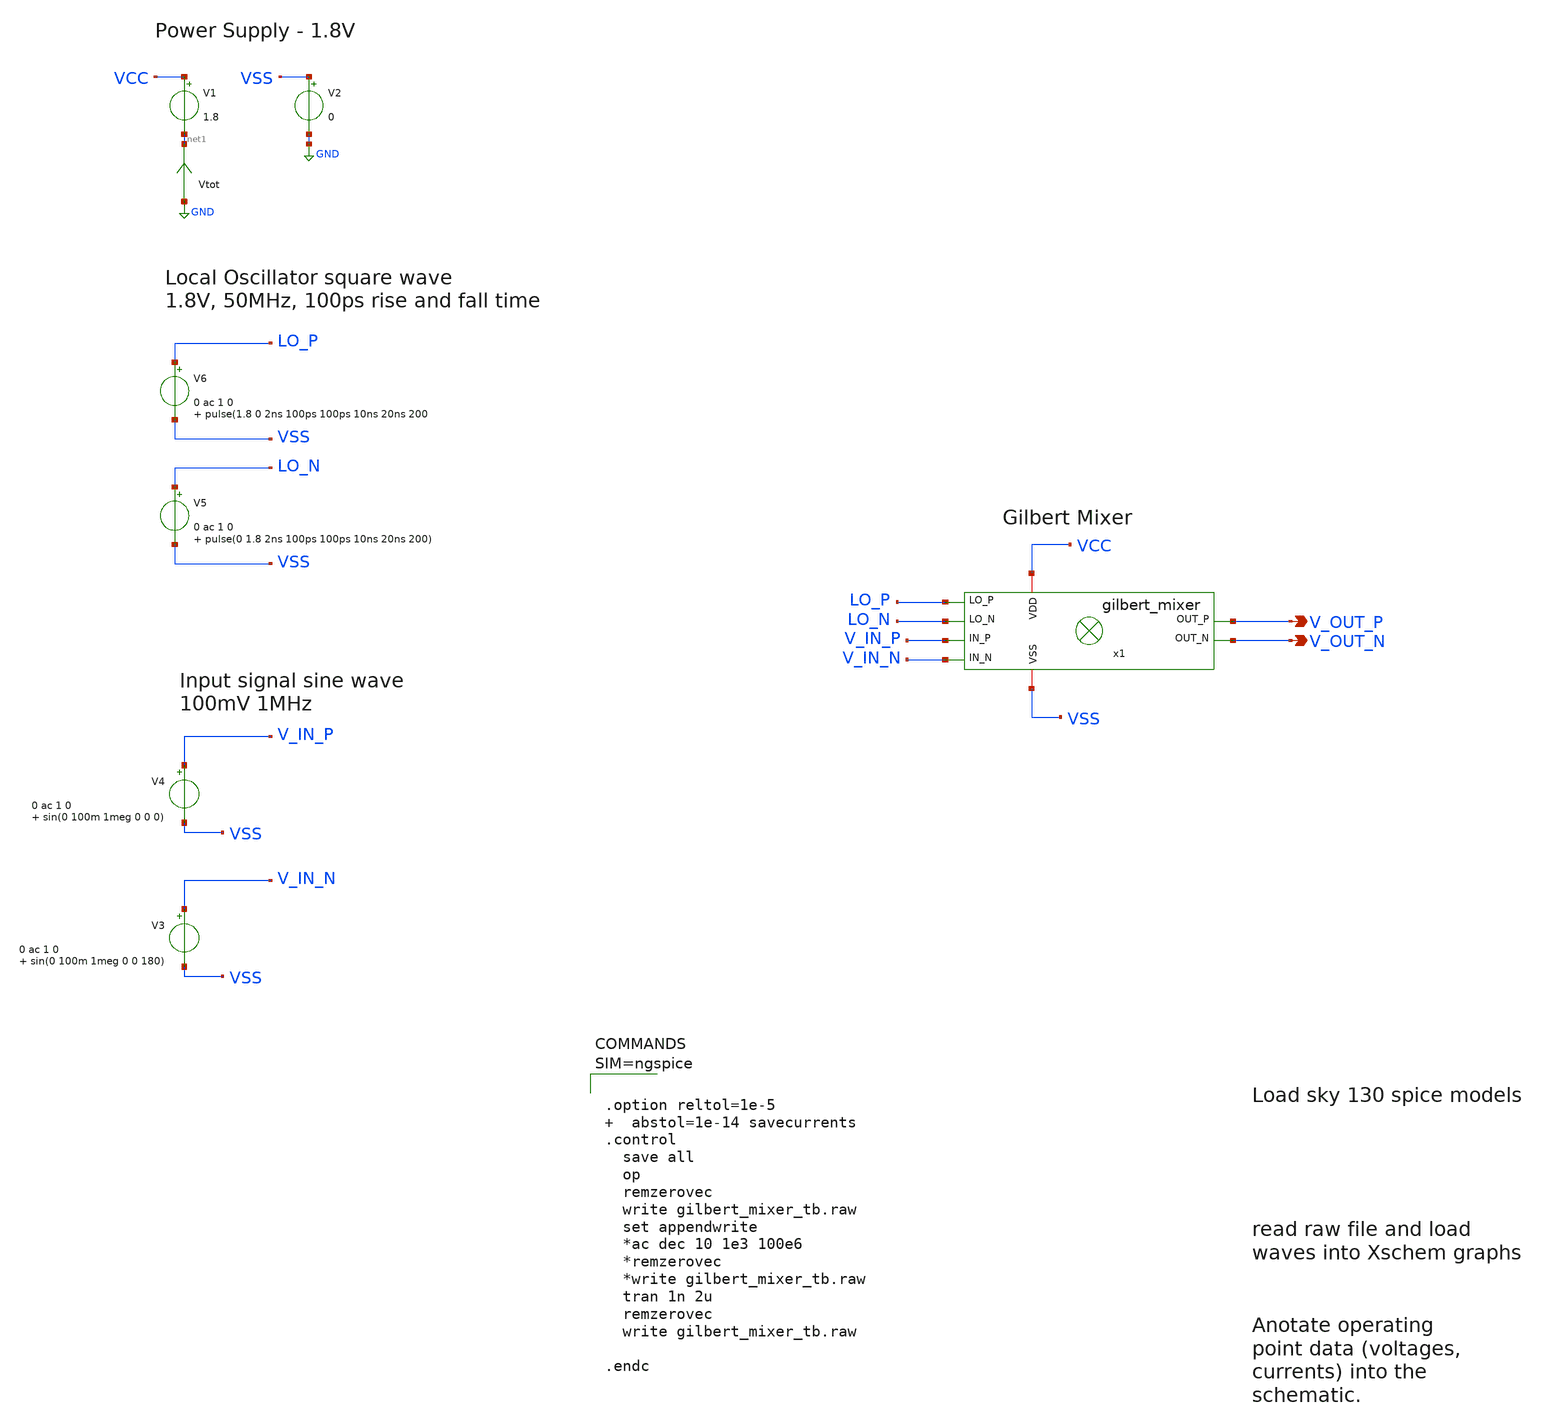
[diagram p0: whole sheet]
** sch_path: xschem/gilbert_mixer_tb.sch
**.subckt gilbert_mixer_tb V_OUT_N V_OUT_P
*.opin V_OUT_N
*.opin V_OUT_P
V1 VCC net1 1.8
V2 VSS GND 0
V4 V_IN_P VSS 0 ac 1 0 sin(0 100m 1meg 0 0 0)
x1 VSS VCC V_OUT_N V_OUT_P LO_N LO_P V_IN_N V_IN_P gilbert_mixer
V5 LO_N VSS 0 ac 1 0 pulse(0 1.8 2ns 100ps 100ps 10ns 20ns 200)
V3 V_IN_N VSS 0 ac 1 0 sin(0 100m 1meg 0 0 180)
Vtot GND net1 0
.save i(vtot)
V6 LO_P VSS 0 ac 1 0 pulse(1.8 0 2ns 100ps 100ps 10ns 20ns 200
**** begin user architecture code

** opencircuitdesign pdks install
.lib $::SKYWATER_MODELS/sky130.lib.spice tt





.option reltol=1e-5   abstol=1e-14 savecurrents
.control
  save all
  op
  remzerovec
  write gilbert_mixer_tb.raw
  set appendwrite
  *ac dec 10 1e3 100e6
  *remzerovec
  *write gilbert_mixer_tb.raw
  tran 1n 2u
  remzerovec
  write gilbert_mixer_tb.raw

.endc



**** end user architecture code
**.ends

* expanding   symbol:  gilbert_mixer.sym # of pins=8
** sym_path: xschem/gilbert_mixer.sym
** sch_path: xschem/gilbert_mixer.sch
.subckt gilbert_mixer VSS VDD OUT_N OUT_P LO_N LO_P IN_N IN_P
*.ipin LO_P
*.ipin LO_N
*.ipin IN_N
*.opin OUT_N
*.opin OUT_P
*.iopin VDD
*.iopin VSS
*.ipin IN_P
XR3 VSS NET_R3 VSS sky130_fd_pr__res_high_po_0p35 L=0.1 mult=30 m=30
XM2 net1 net3 NET_M6_DRAIN VSS sky130_fd_pr__nfet_01v8 L=0.38 W=3.6 nf=2 ad='int((nf+1)/2) * W/nf * 0.29'
+ as='int((nf+2)/2) * W/nf * 0.29' pd='2*int((nf+1)/2) * (W/nf + 0.29)' ps='2*int((nf+2)/2) * (W/nf + 0.29)'
+ nrd='0.29 / W' nrs='0.29 / W' sa=0 sb=0 sd=0 mult=1 m=1
XM4 net2 net3 NET_M5_DRAIN VSS sky130_fd_pr__nfet_01v8 L=0.38 W=3.6 nf=2 ad='int((nf+1)/2) * W/nf * 0.29'
+ as='int((nf+2)/2) * W/nf * 0.29' pd='2*int((nf+1)/2) * (W/nf + 0.29)' ps='2*int((nf+2)/2) * (W/nf + 0.29)'
+ nrd='0.29 / W' nrs='0.29 / W' sa=0 sb=0 sd=0 mult=1 m=1
XM6 NET_M6_DRAIN LO_N NET_R3 VSS sky130_fd_pr__nfet_01v8 L=0.38 W=3.6 nf=2 ad='int((nf+1)/2) * W/nf * 0.29'
+ as='int((nf+2)/2) * W/nf * 0.29' pd='2*int((nf+1)/2) * (W/nf + 0.29)' ps='2*int((nf+2)/2) * (W/nf + 0.29)'
+ nrd='0.29 / W' nrs='0.29 / W' sa=0 sb=0 sd=0 mult=1 m=1
XM1 net2 net4 NET_M6_DRAIN VSS sky130_fd_pr__nfet_01v8 L=0.38 W=3.6 nf=2 ad='int((nf+1)/2) * W/nf * 0.29'
+ as='int((nf+2)/2) * W/nf * 0.29' pd='2*int((nf+1)/2) * (W/nf + 0.29)' ps='2*int((nf+2)/2) * (W/nf + 0.29)'
+ nrd='0.29 / W' nrs='0.29 / W' sa=0 sb=0 sd=0 mult=1 m=1
XM3 net1 net4 NET_M5_DRAIN VSS sky130_fd_pr__nfet_01v8 L=0.38 W=3.6 nf=2 ad='int((nf+1)/2) * W/nf * 0.29'
+ as='int((nf+2)/2) * W/nf * 0.29' pd='2*int((nf+1)/2) * (W/nf + 0.29)' ps='2*int((nf+2)/2) * (W/nf + 0.29)'
+ nrd='0.29 / W' nrs='0.29 / W' sa=0 sb=0 sd=0 mult=1 m=1
XM5 NET_M5_DRAIN LO_P NET_R3 VSS sky130_fd_pr__nfet_01v8 L=0.38 W=3.6 nf=2 ad='int((nf+1)/2) * W/nf * 0.29'
+ as='int((nf+2)/2) * W/nf * 0.29' pd='2*int((nf+1)/2) * (W/nf + 0.29)' ps='2*int((nf+2)/2) * (W/nf + 0.29)'
+ nrd='0.29 / W' nrs='0.29 / W' sa=0 sb=0 sd=0 mult=1 m=1
XR1 net2 VDD VSS sky130_fd_pr__res_high_po_0p35 L=15.3 mult=2 m=2
XR2 net1 VDD VSS sky130_fd_pr__res_high_po_0p35 L=15.3 mult=2 m=2
XR4 net3 VDD VSS sky130_fd_pr__res_high_po_0p35 L=6 mult=2 m=2
XR5 VSS net3 VSS sky130_fd_pr__res_high_po_0p35 L=7 mult=2 m=2
XC1 net3 IN_N sky130_fd_pr__cap_mim_m3_2 W=200 L=200 MF=4 m=4
XR6 net4 VDD VSS sky130_fd_pr__res_high_po_0p35 L=6 mult=2 m=2
XR7 VSS net4 VSS sky130_fd_pr__res_high_po_0p35 L=7 mult=2 m=2
XC2 net4 IN_P sky130_fd_pr__cap_mim_m3_2 W=200 L=200 MF=4 m=4
XC3 net1 OUT_P sky130_fd_pr__cap_mim_m3_2 W=200 L=200 MF=4 m=4
XC4 net2 OUT_N sky130_fd_pr__cap_mim_m3_2 W=200 L=200 MF=4 m=4
.ends

.GLOBAL GND
.end
